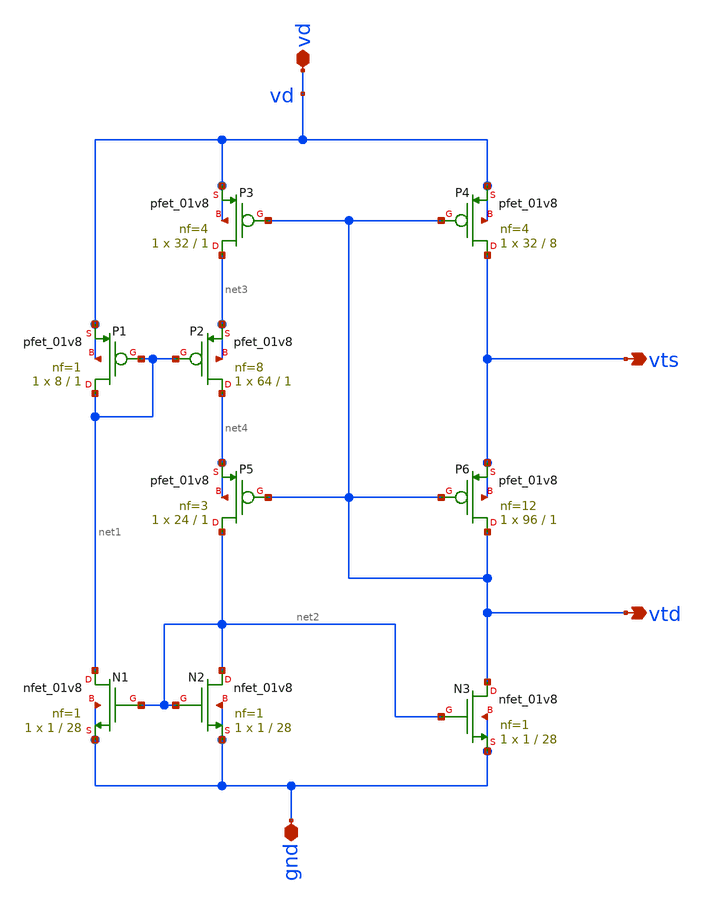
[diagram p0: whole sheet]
** sch_path: sensor/xschem/sensor.sch
**.subckt sensor vd gnd vts vtd
*.iopin vd
*.iopin gnd
*.opin vts
*.opin vtd
XP6 vtd vtd vts vts sky130_fd_pr__pfet_01v8 L=1 W=96 nf=12 ad='int((nf+1)/2) * W/nf * 0.29' as='int((nf+2)/2) * W/nf * 0.29'
+ pd='2*int((nf+1)/2) * (W/nf + 0.29)' ps='2*int((nf+2)/2) * (W/nf + 0.29)' nrd='0.29 / W' nrs='0.29 / W'
+ sa=0 sb=0 sd=0 mult=1 m=1
XN1 net1 net2 gnd gnd sky130_fd_pr__nfet_01v8 L=28 W=1 nf=1 ad='int((nf+1)/2) * W/nf * 0.29' as='int((nf+2)/2) * W/nf * 0.29'
+ pd='2*int((nf+1)/2) * (W/nf + 0.29)' ps='2*int((nf+2)/2) * (W/nf + 0.29)' nrd='0.29 / W' nrs='0.29 / W'
+ sa=0 sb=0 sd=0 mult=1 m=1
XP3 net3 vtd vd vd sky130_fd_pr__pfet_01v8 L=1 W=32 nf=4 ad='int((nf+1)/2) * W/nf * 0.29' as='int((nf+2)/2) * W/nf * 0.29'
+ pd='2*int((nf+1)/2) * (W/nf + 0.29)' ps='2*int((nf+2)/2) * (W/nf + 0.29)' nrd='0.29 / W' nrs='0.29 / W'
+ sa=0 sb=0 sd=0 mult=1 m=1
XP1 net1 net1 vd vd sky130_fd_pr__pfet_01v8 L=1 W=8 nf=1 ad='int((nf+1)/2) * W/nf * 0.29' as='int((nf+2)/2) * W/nf * 0.29'
+ pd='2*int((nf+1)/2) * (W/nf + 0.29)' ps='2*int((nf+2)/2) * (W/nf + 0.29)' nrd='0.29 / W' nrs='0.29 / W'
+ sa=0 sb=0 sd=0 mult=1 m=1
XP2 net4 net1 net3 net3 sky130_fd_pr__pfet_01v8 L=1 W=64 nf=8 ad='int((nf+1)/2) * W/nf * 0.29' as='int((nf+2)/2) * W/nf * 0.29'
+ pd='2*int((nf+1)/2) * (W/nf + 0.29)' ps='2*int((nf+2)/2) * (W/nf + 0.29)' nrd='0.29 / W' nrs='0.29 / W'
+ sa=0 sb=0 sd=0 mult=1 m=1
XP4 vts vtd vd vd sky130_fd_pr__pfet_01v8 L=8 W=32 nf=4 ad='int((nf+1)/2) * W/nf * 0.29' as='int((nf+2)/2) * W/nf * 0.29'
+ pd='2*int((nf+1)/2) * (W/nf + 0.29)' ps='2*int((nf+2)/2) * (W/nf + 0.29)' nrd='0.29 / W' nrs='0.29 / W'
+ sa=0 sb=0 sd=0 mult=1 m=1
XN2 net2 net2 gnd gnd sky130_fd_pr__nfet_01v8 L=28 W=1 nf=1 ad='int((nf+1)/2) * W/nf * 0.29' as='int((nf+2)/2) * W/nf * 0.29'
+ pd='2*int((nf+1)/2) * (W/nf + 0.29)' ps='2*int((nf+2)/2) * (W/nf + 0.29)' nrd='0.29 / W' nrs='0.29 / W'
+ sa=0 sb=0 sd=0 mult=1 m=1
XN3 vtd net2 gnd gnd sky130_fd_pr__nfet_01v8 L=28 W=1 nf=1 ad='int((nf+1)/2) * W/nf * 0.29' as='int((nf+2)/2) * W/nf * 0.29'
+ pd='2*int((nf+1)/2) * (W/nf + 0.29)' ps='2*int((nf+2)/2) * (W/nf + 0.29)' nrd='0.29 / W' nrs='0.29 / W'
+ sa=0 sb=0 sd=0 mult=1 m=1
XP5 net2 vtd net4 net4 sky130_fd_pr__pfet_01v8 L=1 W=24 nf=3 ad='int((nf+1)/2) * W/nf * 0.29' as='int((nf+2)/2) * W/nf * 0.29'
+ pd='2*int((nf+1)/2) * (W/nf + 0.29)' ps='2*int((nf+2)/2) * (W/nf + 0.29)' nrd='0.29 / W' nrs='0.29 / W'
+ sa=0 sb=0 sd=0 mult=1 m=1
**.ends
.end
